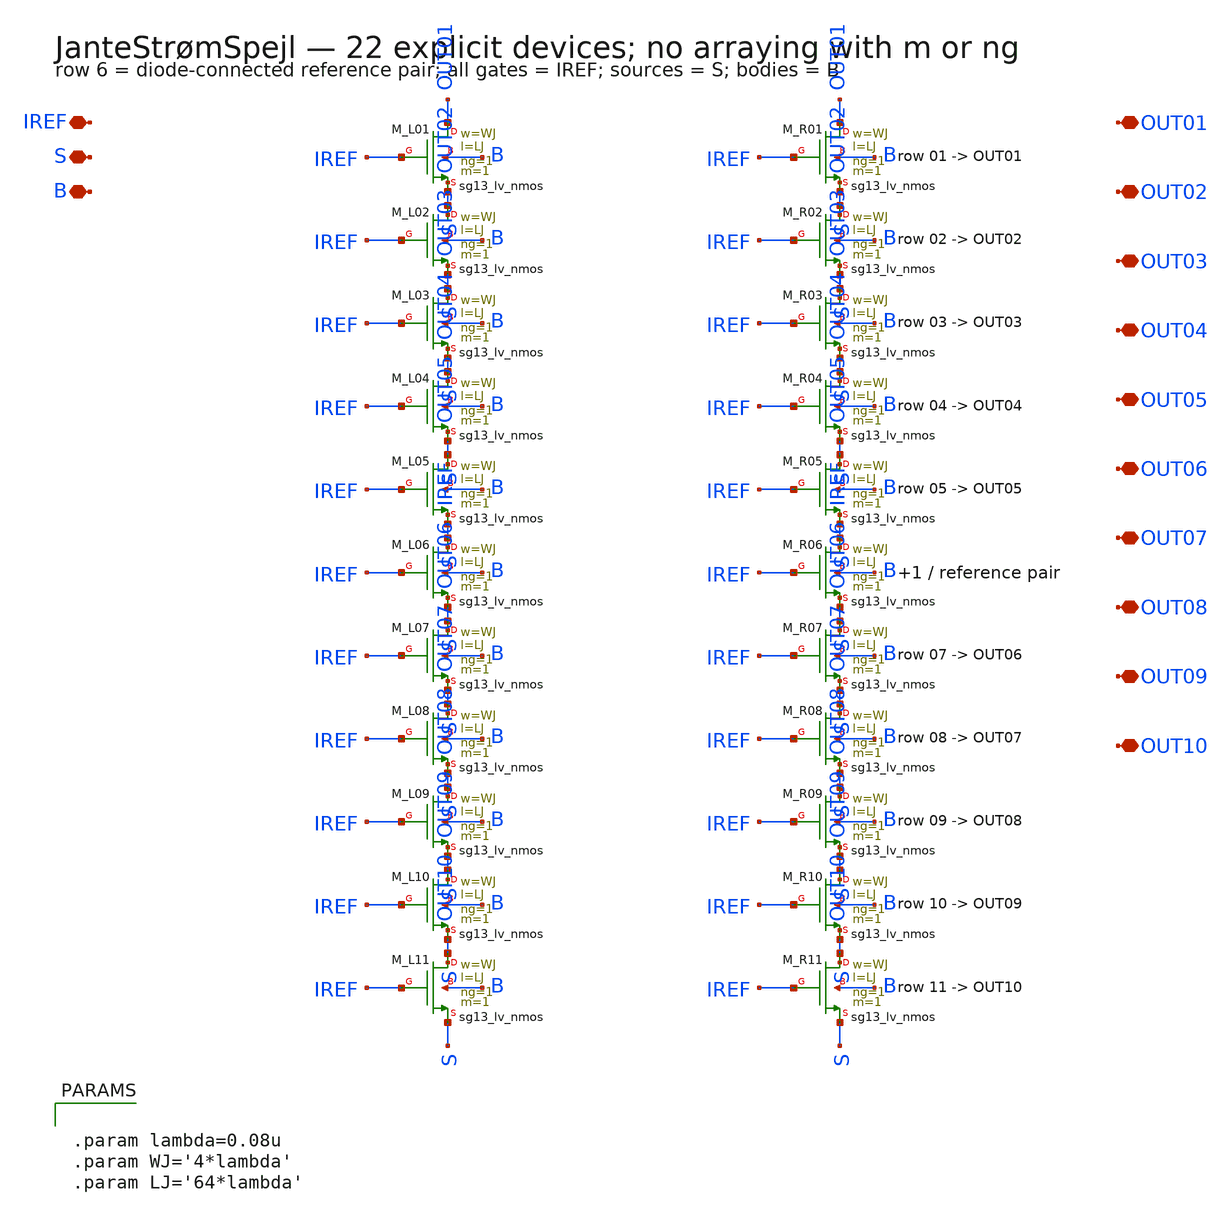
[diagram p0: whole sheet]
** sch_path: sudelbuecher/JanteStroemSpejl/JanteStroemSpejl.sch
**.subckt JanteStroemSpejl IREF S B OUT01 OUT02 OUT03 OUT04 OUT05 OUT06 OUT07 OUT08 OUT09 OUT10
*.iopin IREF
*.iopin S
*.iopin B
*.iopin OUT01
*.iopin OUT02
*.iopin OUT03
*.iopin OUT04
*.iopin OUT05
*.iopin OUT06
*.iopin OUT07
*.iopin OUT08
*.iopin OUT09
*.iopin OUT10
XM_L01 OUT01 IREF S B sg13_lv_nmos w=WJ l=LJ ng=1 m=1 mm_ok=1
XM_R01 OUT01 IREF S B sg13_lv_nmos w=WJ l=LJ ng=1 m=1 mm_ok=1
XM_L02 S IREF S B sg13_lv_nmos w=WJ l=LJ ng=1 m=1 mm_ok=1
XM_R02 S IREF S B sg13_lv_nmos w=WJ l=LJ ng=1 m=1 mm_ok=1
XM_L03 S IREF S B sg13_lv_nmos w=WJ l=LJ ng=1 m=1 mm_ok=1
XM_R03 S IREF S B sg13_lv_nmos w=WJ l=LJ ng=1 m=1 mm_ok=1
XM_L04 S IREF S B sg13_lv_nmos w=WJ l=LJ ng=1 m=1 mm_ok=1
XM_R04 S IREF S B sg13_lv_nmos w=WJ l=LJ ng=1 m=1 mm_ok=1
XM_L05 S IREF S B sg13_lv_nmos w=WJ l=LJ ng=1 m=1 mm_ok=1
XM_R05 S IREF S B sg13_lv_nmos w=WJ l=LJ ng=1 m=1 mm_ok=1
XM_L06 S IREF S B sg13_lv_nmos w=WJ l=LJ ng=1 m=1 mm_ok=1
XM_R06 S IREF S B sg13_lv_nmos w=WJ l=LJ ng=1 m=1 mm_ok=1
XM_L07 S IREF S B sg13_lv_nmos w=WJ l=LJ ng=1 m=1 mm_ok=1
XM_R07 S IREF S B sg13_lv_nmos w=WJ l=LJ ng=1 m=1 mm_ok=1
XM_L08 S IREF S B sg13_lv_nmos w=WJ l=LJ ng=1 m=1 mm_ok=1
XM_R08 S IREF S B sg13_lv_nmos w=WJ l=LJ ng=1 m=1 mm_ok=1
XM_L09 S IREF S B sg13_lv_nmos w=WJ l=LJ ng=1 m=1 mm_ok=1
XM_R09 S IREF S B sg13_lv_nmos w=WJ l=LJ ng=1 m=1 mm_ok=1
XM_L10 S IREF S B sg13_lv_nmos w=WJ l=LJ ng=1 m=1 mm_ok=1
XM_R10 S IREF S B sg13_lv_nmos w=WJ l=LJ ng=1 m=1 mm_ok=1
XM_L11 S IREF S B sg13_lv_nmos w=WJ l=LJ ng=1 m=1 mm_ok=1
XM_R11 S IREF S B sg13_lv_nmos w=WJ l=LJ ng=1 m=1 mm_ok=1
**** begin user architecture code


.param lambda=0.08u
.param WJ='4*lambda'
.param LJ='64*lambda'


**** end user architecture code
**.ends
.end
